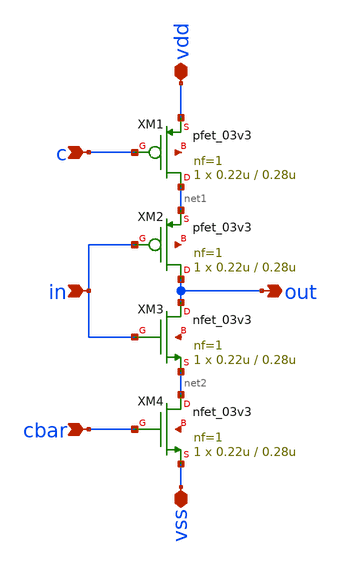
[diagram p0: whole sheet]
** sch_path: tristate.sch
**.subckt tristate in out vdd vss c cbar
*.ipin in
*.opin out
*.iopin vdd
*.iopin vss
*.ipin c
*.ipin cbar
XM1 net1 c vdd net3 pfet_03v3 L=0.28u W=0.22u nf=1 ad='int((nf+1)/2) * W/nf * 0.18u' as='int((nf+2)/2) * W/nf * 0.18u'
+ pd='2*int((nf+1)/2) * (W/nf + 0.18u)' ps='2*int((nf+2)/2) * (W/nf + 0.18u)' nrd='0.18u / W' nrs='0.18u / W'
+ sa=0 sb=0 sd=0 m=1
XM2 out in net1 net4 pfet_03v3 L=0.28u W=0.22u nf=1 ad='int((nf+1)/2) * W/nf * 0.18u' as='int((nf+2)/2) * W/nf * 0.18u'
+ pd='2*int((nf+1)/2) * (W/nf + 0.18u)' ps='2*int((nf+2)/2) * (W/nf + 0.18u)' nrd='0.18u / W' nrs='0.18u / W'
+ sa=0 sb=0 sd=0 m=1
XM3 out in net2 net5 nfet_03v3 L=0.28u W=0.22u nf=1 ad='int((nf+1)/2) * W/nf * 0.18u' as='int((nf+2)/2) * W/nf * 0.18u'
+ pd='2*int((nf+1)/2) * (W/nf + 0.18u)' ps='2*int((nf+2)/2) * (W/nf + 0.18u)' nrd='0.18u / W' nrs='0.18u / W'
+ sa=0 sb=0 sd=0 m=1
XM4 net2 cbar vss net6 nfet_03v3 L=0.28u W=0.22u nf=1 ad='int((nf+1)/2) * W/nf * 0.18u' as='int((nf+2)/2) * W/nf * 0.18u'
+ pd='2*int((nf+1)/2) * (W/nf + 0.18u)' ps='2*int((nf+2)/2) * (W/nf + 0.18u)' nrd='0.18u / W' nrs='0.18u / W'
+ sa=0 sb=0 sd=0 m=1
**.ends
.end
